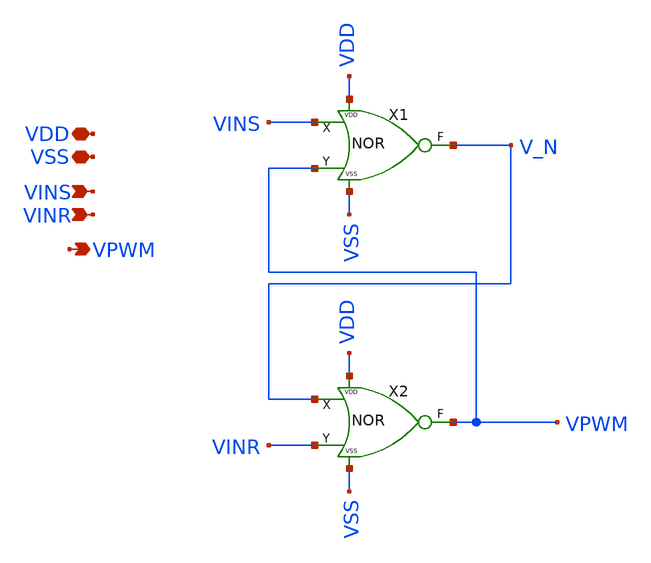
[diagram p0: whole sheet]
** sch_path: xschem/SR_Latch_NOR/SR_Latch.sch
**.subckt SR_Latch VDD VINS VSS VPWM VINR
*.iopin VDD
*.ipin VINS
*.iopin VSS
*.opin VPWM
*.ipin VINR
X1 VDD VSS V_N VINS VPWM NOR
X2 VDD VSS VPWM V_N VINR NOR
**** begin user architecture code



**** end user architecture code
**.ends

* expanding   symbol:  ../DigitalGates/NOR.sym # of pins=5
** sym_path: xschem/DigitalGates/NOR.sym
** sch_path: xschem/DigitalGates/NOR.sch
.subckt NOR VDD VSS F X Y
*.iopin VDD
*.ipin X
*.opin F
*.iopin VSS
*.ipin Y
XM1 F Y VSS VSS sg13_lv_nmos w={w_N_NOR} l={l_N_NOR} ng=1 m={mult} mm_ok=1
XM2 net1 X VDD VDD sg13_lv_pmos w={w_P_NOR} l={l_P_NOR} ng=1 m={mult*3} mm_ok=1
XM4 F Y net1 VDD sg13_lv_pmos w={w_P_NOR} l={l_P_NOR} ng=1 m={mult*3} mm_ok=1
XM3 F X VSS VSS sg13_lv_nmos w={w_N_NOR} l={l_N_NOR} ng=1 m={mult} mm_ok=1
**** begin user architecture code



**** end user architecture code
.ends

.end
